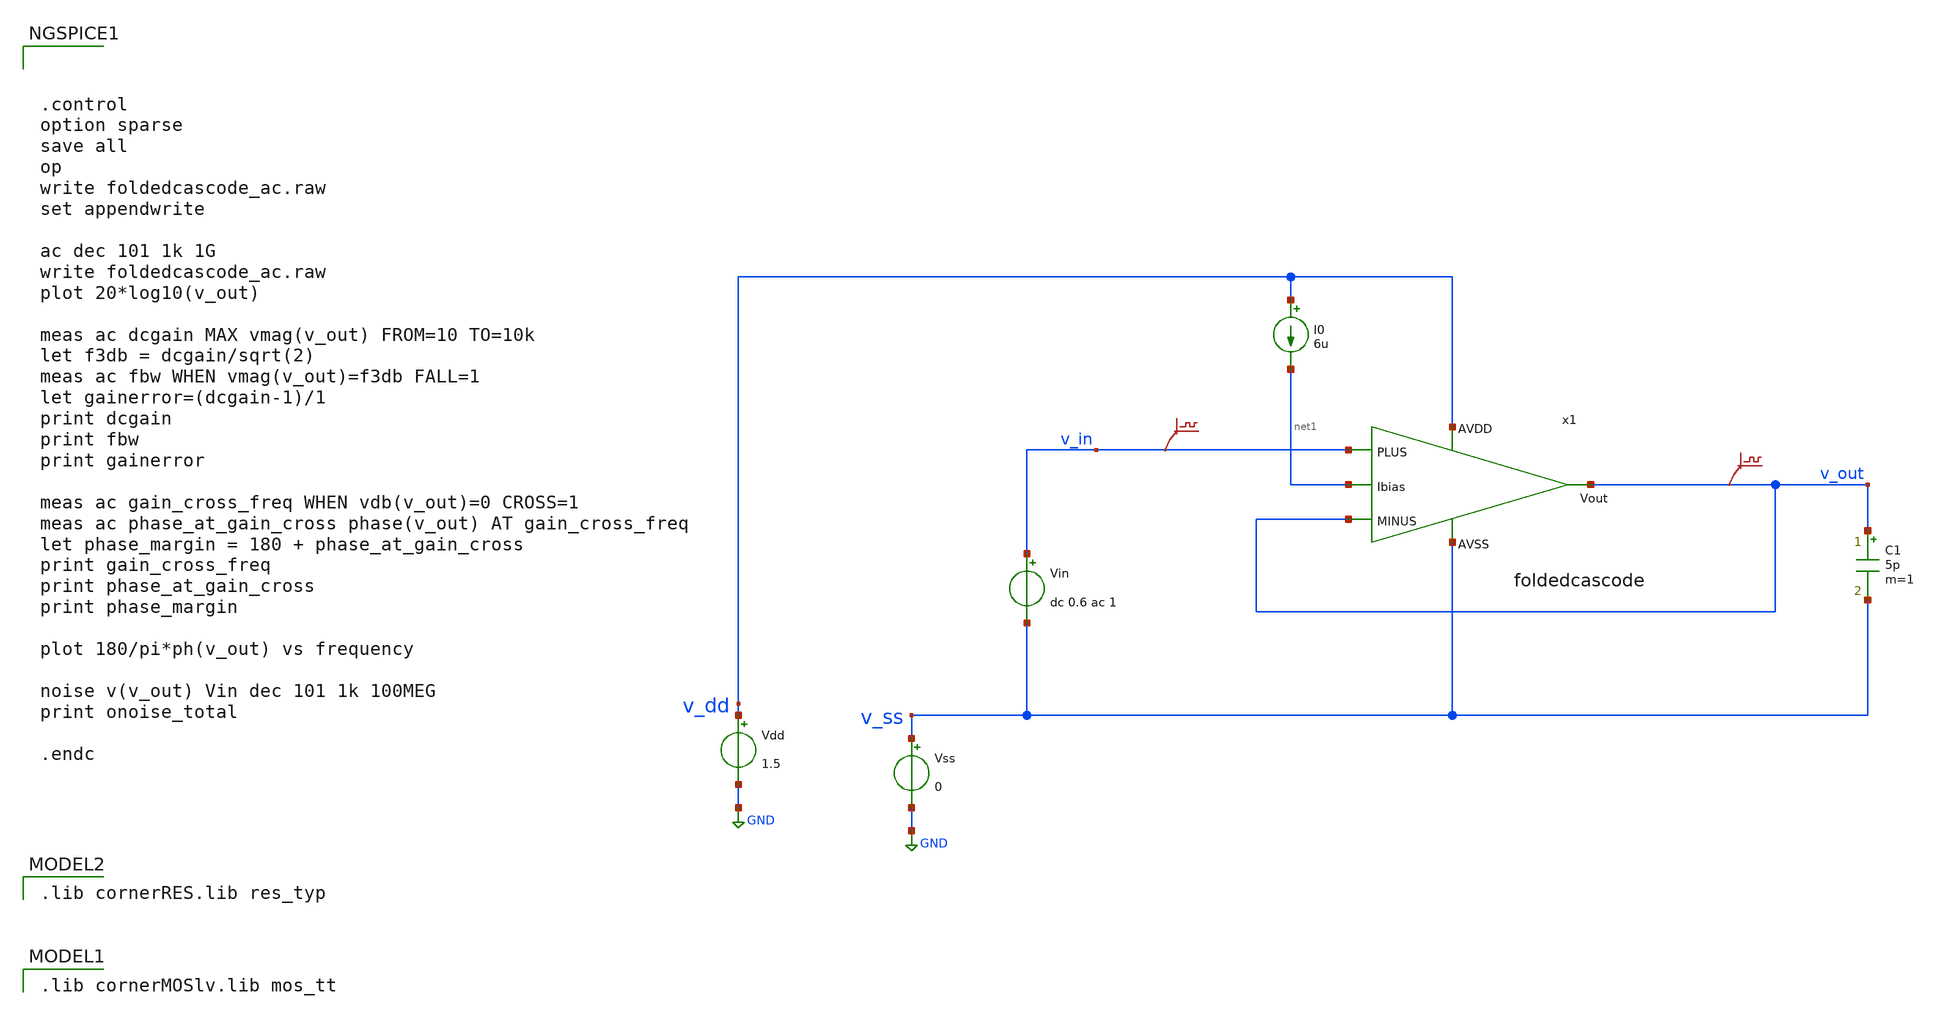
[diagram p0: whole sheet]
** sch_path: Designs/5t_ota/tb_foldedcascode_ac.sch
* (c) 2025 Thesis_HP, Apache-2.0 license
**.subckt tb_foldedcascode_ac
Vss v_ss GND 0
Vdd v_dd GND 1.5
Vin v_in v_ss dc 0.6 ac 1
.save v(v_in)
I0 v_dd net1 6u
C1 v_out v_ss 5p m=1
.save v(v_out)
x1 v_dd net1 v_in v_out v_out v_ss foldedcascode
**** begin user architecture code
 .lib cornerMOSlv.lib mos_tt

 .lib cornerRES.lib res_typ




.control
option sparse
save all
op
write foldedcascode_ac.raw
set appendwrite

ac dec 101 1k 1G
write foldedcascode_ac.raw
plot 20*log10(v_out)

meas ac dcgain MAX vmag(v_out) FROM=10 TO=10k
let f3db = dcgain/sqrt(2)
meas ac fbw WHEN vmag(v_out)=f3db FALL=1
let gainerror=(dcgain-1)/1
print dcgain
print fbw
print gainerror

meas ac gain_cross_freq WHEN vdb(v_out)=0 CROSS=1
meas ac phase_at_gain_cross phase(v_out) AT gain_cross_freq
let phase_margin = 180 + phase_at_gain_cross
print gain_cross_freq
print phase_at_gain_cross
print phase_margin

plot 180/pi*ph(v_out) vs frequency

noise v(v_out) Vin dec 101 1k 100MEG
print onoise_total

.endc


**** end user architecture code
**.ends

* expanding   symbol:  foldedcascode.sym # of pins=6
** sym_path: Designs/otas/foldedcascode.sym
** sch_path: Designs/otas/foldedcascode.sch
.subckt foldedcascode AVDD Ibias PLUS MINUS Vout AVSS
*.ipin AVDD
*.ipin AVSS
*.ipin PLUS
*.ipin MINUS
*.opin Vout
*.ipin Ibias
XMt2 net1 Ibias AVDD AVDD sg13_lv_pmos w=21u l=1u ng=3 m=1 mm_ok=1
XM1 net3 PLUS net1 AVDD sg13_lv_pmos w=19.5u l=1u ng=2 m=1 mm_ok=1
XM2 net8 MINUS net1 AVDD sg13_lv_pmos w=19.5u l=1u ng=2 m=1 mm_ok=1
XM6 net6 Vout AVDD AVDD sg13_lv_pmos w=3u l=0.5u ng=1 m=1 mm_ok=1
XM7 net5 net4 net6 AVDD sg13_lv_pmos w=5u l=0.5u ng=2 m=1 mm_ok=1
XM8 net7 Vout AVDD AVDD sg13_lv_pmos w=3u l=0.5u ng=1 m=1 mm_ok=1
XM15 Vout net4 net7 AVDD sg13_lv_pmos w=5u l=0.5u ng=2 m=1 mm_ok=1
XM16 Vout Ibias net8 AVSS sg13_lv_nmos w=1.5u l=0.5u ng=1 m=1 mm_ok=1
XM17 net8 net2 AVSS AVSS sg13_lv_nmos w=1.5u l=0.5u ng=1 m=1 mm_ok=1
XM18 net5 Ibias net3 AVSS sg13_lv_nmos w=1.5u l=0.5u ng=1 m=1 mm_ok=1
XM27 net3 net2 AVSS AVSS sg13_lv_nmos w=1.5u l=0.5u ng=1 m=1 mm_ok=1
XM28 Ibias Ibias AVDD AVDD sg13_lv_pmos w=15u l=1u ng=3 m=1 mm_ok=1
XM29 Ibias Ibias net2 AVSS sg13_lv_nmos w=3u l=0.5u ng=1 m=1 mm_ok=1
XM30 net2 net2 AVSS AVSS sg13_lv_nmos w=3u l=0.5u ng=1 m=1 mm_ok=1
XM31 AVDD Ibias net9 AVSS sg13_lv_nmos w=3u l=0.5u ng=1 m=1 mm_ok=1
XM32 net9 net2 AVSS AVSS sg13_lv_nmos w=3u l=0.5u ng=1 m=1 mm_ok=1
XM33 net4 net2 AVSS AVSS sg13_lv_nmos w=3u l=0.5u ng=1 m=1 mm_ok=1
XM34 net4 net4 AVDD AVDD sg13_lv_pmos w=10u l=0.5u ng=2 m=1 mm_ok=1
XMdecoup1 AVDD net4 AVDD AVDD sg13_lv_pmos w=12u l=0.5u ng=4 m=1 mm_ok=1
XMdecoup2 AVDD Ibias AVDD AVDD sg13_lv_pmos w=12u l=0.5u ng=4 m=1 mm_ok=1
XMdecoup3 AVSS Ibias AVSS AVSS sg13_lv_nmos w=8u l=1u ng=4 m=1 mm_ok=1
XMdecoup4 AVSS net2 AVSS AVSS sg13_lv_nmos w=8u l=1u ng=4 m=1 mm_ok=1
XMdecoup5 AVSS net2 AVSS AVSS sg13_lv_nmos w=8u l=1u ng=4 m=1 mm_ok=1
.ends

.GLOBAL GND
.end
